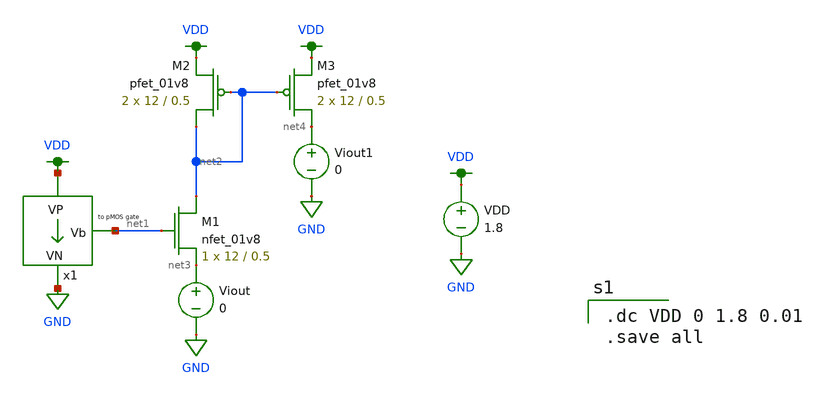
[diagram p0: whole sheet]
** sch_path: schematics/bias/test_current_bias.sch
**.subckt test_current_bias
x1 VDD net1 GND current_bias
VDD VDD GND 1.8
XM1 net2 net1 net3 GND sky130_fd_pr__nfet_01v8 L=0.5 W=12 nf=1 ad='int((nf+1)/2) * W/nf * 0.29' as='int((nf+2)/2) * W/nf * 0.29'
+ pd='2*int((nf+1)/2) * (W/nf + 0.29)' ps='2*int((nf+2)/2) * (W/nf + 0.29)' nrd='0.29 / W' nrs='0.29 / W'
+ sa=0 sb=0 sd=0 mult=1 m=1
Viout net3 GND 0
XM2 net2 net2 VDD VDD sky130_fd_pr__pfet_01v8 L=0.5 W=12 nf=1 ad='int((nf+1)/2) * W/nf * 0.29' as='int((nf+2)/2) * W/nf * 0.29'
+ pd='2*int((nf+1)/2) * (W/nf + 0.29)' ps='2*int((nf+2)/2) * (W/nf + 0.29)' nrd='0.29 / W' nrs='0.29 / W'
+ sa=0 sb=0 sd=0 mult=2 m=2
XM3 net4 net2 VDD VDD sky130_fd_pr__pfet_01v8 L=0.5 W=12 nf=1 ad='int((nf+1)/2) * W/nf * 0.29' as='int((nf+2)/2) * W/nf * 0.29'
+ pd='2*int((nf+1)/2) * (W/nf + 0.29)' ps='2*int((nf+2)/2) * (W/nf + 0.29)' nrd='0.29 / W' nrs='0.29 / W'
+ sa=0 sb=0 sd=0 mult=2 m=2
Viout1 net4 GND 0
**** begin user architecture code

.option wnflag=1
.param MC_SWITCH=0.0
.lib ~/skywater/skywater-pdk/libraries/sky130_fd_pr_ngspice/latest/models/sky130.lib.spice tt


.dc VDD 0 1.8 0.01
.save all

**** end user architecture code
**.ends

* expanding   symbol:
*+  /home/madvlsi/dev/git/7-bit-D-A-converter-MP4-MADVLSI/schematics/bias/current_bias.sym # of pins=3
** sym_path: schematics/bias_2/current_bias.sym
** sch_path: schematics/bias_2/current_bias.sch
.subckt current_bias VP Vb VN
*.iopin VP
*.iopin VN
*.opin Vb
XM4 net1 net1 net4 GND sky130_fd_pr__nfet_01v8 L=0.5 W=12 nf=1 ad='int((nf+1)/2) * W/nf * 0.29' as='int((nf+2)/2) * W/nf * 0.29'
+ pd='2*int((nf+1)/2) * (W/nf + 0.29)' ps='2*int((nf+2)/2) * (W/nf + 0.29)' nrd='0.29 / W' nrs='0.29 / W'
+ sa=0 sb=0 sd=0 mult=8 m=8
XM5 net3 net1 VN GND sky130_fd_pr__nfet_01v8 L=0.5 W=12 nf=1 ad='int((nf+1)/2) * W/nf * 0.29' as='int((nf+2)/2) * W/nf * 0.29'
+ pd='2*int((nf+1)/2) * (W/nf + 0.29)' ps='2*int((nf+2)/2) * (W/nf + 0.29)' nrd='0.29 / W' nrs='0.29 / W'
+ sa=0 sb=0 sd=0 mult=1 m=1
XM6 Vb net2 VN GND sky130_fd_pr__nfet_01v8 L=0.5 W=12 nf=1 ad='int((nf+1)/2) * W/nf * 0.29' as='int((nf+2)/2) * W/nf * 0.29'
+ pd='2*int((nf+1)/2) * (W/nf + 0.29)' ps='2*int((nf+2)/2) * (W/nf + 0.29)' nrd='0.29 / W' nrs='0.29 / W'
+ sa=0 sb=0 sd=0 mult=1 m=1
XM7 net2 net2 VN GND sky130_fd_pr__nfet_01v8 L=0.5 W=12 nf=1 ad='int((nf+1)/2) * W/nf * 0.29' as='int((nf+2)/2) * W/nf * 0.29'
+ pd='2*int((nf+1)/2) * (W/nf + 0.29)' ps='2*int((nf+2)/2) * (W/nf + 0.29)' nrd='0.29 / W' nrs='0.29 / W'
+ sa=0 sb=0 sd=0 mult=1 m=1
R1 net4 VN 100k m=1
XM8 Vb net3 VP VDD sky130_fd_pr__pfet_01v8 L=0.5 W=12 nf=1 ad='int((nf+1)/2) * W/nf * 0.29' as='int((nf+2)/2) * W/nf * 0.29'
+ pd='2*int((nf+1)/2) * (W/nf + 0.29)' ps='2*int((nf+2)/2) * (W/nf + 0.29)' nrd='0.29 / W' nrs='0.29 / W'
+ sa=0 sb=0 sd=0 mult=1 m=1
XM9 net2 Vb VP VDD sky130_fd_pr__pfet_01v8 L=0.5 W=12 nf=1 ad='int((nf+1)/2) * W/nf * 0.29' as='int((nf+2)/2) * W/nf * 0.29'
+ pd='2*int((nf+1)/2) * (W/nf + 0.29)' ps='2*int((nf+2)/2) * (W/nf + 0.29)' nrd='0.29 / W' nrs='0.29 / W'
+ sa=0 sb=0 sd=0 mult=1 m=1
XM10 net3 net3 VP VDD sky130_fd_pr__pfet_01v8 L=0.5 W=12 nf=1 ad='int((nf+1)/2) * W/nf * 0.29' as='int((nf+2)/2) * W/nf * 0.29'
+ pd='2*int((nf+1)/2) * (W/nf + 0.29)' ps='2*int((nf+2)/2) * (W/nf + 0.29)' nrd='0.29 / W' nrs='0.29 / W'
+ sa=0 sb=0 sd=0 mult=1 m=1
XM11 net1 Vb VP VDD sky130_fd_pr__pfet_01v8 L=0.5 W=12 nf=1 ad='int((nf+1)/2) * W/nf * 0.29' as='int((nf+2)/2) * W/nf * 0.29'
+ pd='2*int((nf+1)/2) * (W/nf + 0.29)' ps='2*int((nf+2)/2) * (W/nf + 0.29)' nrd='0.29 / W' nrs='0.29 / W'
+ sa=0 sb=0 sd=0 mult=1 m=1
.ends

.GLOBAL VDD
.GLOBAL GND
.end
